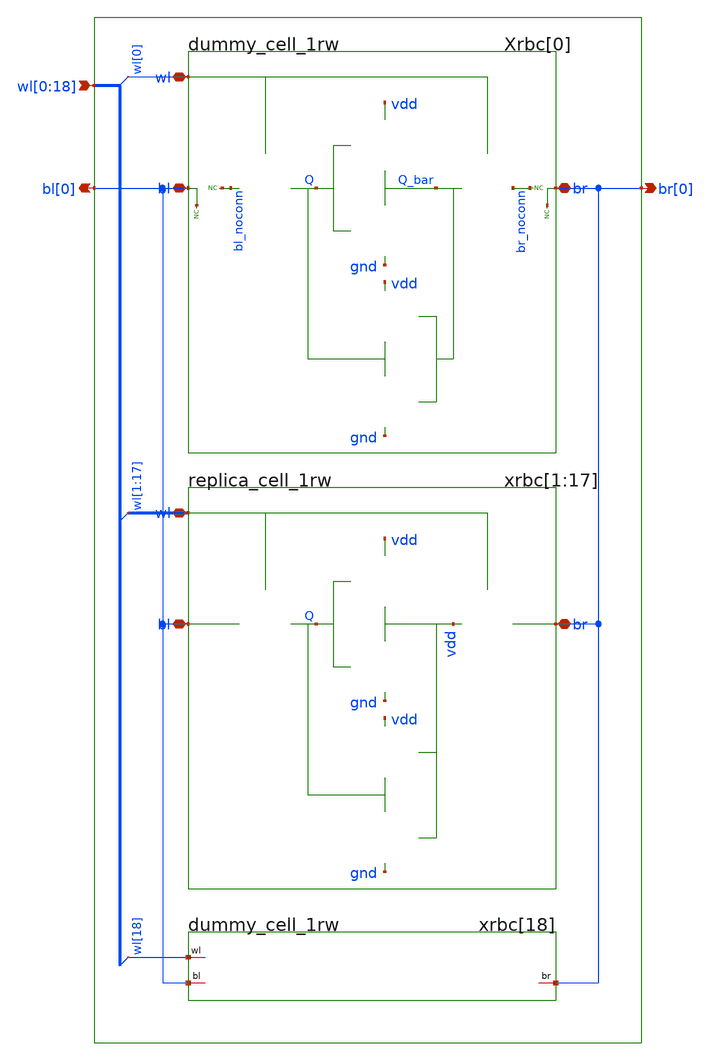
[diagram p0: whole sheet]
** sch_path: sram_4_16_scn4m/replica_column.sch
**.subckt replica_column bl[0] br[0]
*+ wl[0],wl[1],wl[2],wl[3],wl[4],wl[5],wl[6],wl[7],wl[8],wl[9],wl[10],wl[11],wl[12],wl[13],wl[14],wl[15],wl[16],wl[17],wl[18]
*.opin bl[0]
*.opin br[0]
*.ipin
*+ wl[0],wl[1],wl[2],wl[3],wl[4],wl[5],wl[6],wl[7],wl[8],wl[9],wl[10],wl[11],wl[12],wl[13],wl[14],wl[15],wl[16],wl[17],wl[18]
Xrbc[0] bl[0] br[0] wl[0] vdd gnd dummy_cell_1rw
xrbc[1] bl[0] br[0] wl[1] vdd gnd replica_cell_1rw
xrbc[2] bl[0] br[0] wl[2] vdd gnd replica_cell_1rw
xrbc[3] bl[0] br[0] wl[3] vdd gnd replica_cell_1rw
xrbc[4] bl[0] br[0] wl[4] vdd gnd replica_cell_1rw
xrbc[5] bl[0] br[0] wl[5] vdd gnd replica_cell_1rw
xrbc[6] bl[0] br[0] wl[6] vdd gnd replica_cell_1rw
xrbc[7] bl[0] br[0] wl[7] vdd gnd replica_cell_1rw
xrbc[8] bl[0] br[0] wl[8] vdd gnd replica_cell_1rw
xrbc[9] bl[0] br[0] wl[9] vdd gnd replica_cell_1rw
xrbc[10] bl[0] br[0] wl[10] vdd gnd replica_cell_1rw
xrbc[11] bl[0] br[0] wl[11] vdd gnd replica_cell_1rw
xrbc[12] bl[0] br[0] wl[12] vdd gnd replica_cell_1rw
xrbc[13] bl[0] br[0] wl[13] vdd gnd replica_cell_1rw
xrbc[14] bl[0] br[0] wl[14] vdd gnd replica_cell_1rw
xrbc[15] bl[0] br[0] wl[15] vdd gnd replica_cell_1rw
xrbc[16] bl[0] br[0] wl[16] vdd gnd replica_cell_1rw
xrbc[17] bl[0] br[0] wl[17] vdd gnd replica_cell_1rw
xrbc[18] bl[0] br[0] wl[18] vdd gnd dummy_cell_1rw
**.ends

* expanding   symbol:  dummy_cell_1rw.sch # of pins=3
** sym_path: sram_4_16_scn4m/dummy_cell_1rw.sch
** sch_path: sram_4_16_scn4m/dummy_cell_1rw.sch
.subckt dummy_cell_1rw bl br wl vdd gnd
*.iopin bl
*.iopin br
*.iopin wl
XM1004 Q wl bl_noconn gnd sky130_fd_pr__nfet_01v8 L=0.4 W=0.8 nf=1 ad='int((nf+1)/2) * W/nf * 0.29' as='int((nf+2)/2) * W/nf * 0.29'
+ pd='2*int((nf+1)/2) * (W/nf + 0.29)' ps='2*int((nf+2)/2) * (W/nf + 0.29)' nrd='0.29 / W' nrs='0.29 / W'
+ sa=0 sb=0 sd=0 mult=1 m=1
XM1001 Q_bar Q vdd vdd sky130_fd_pr__pfet_01v8 L=0.8 W=0.6 nf=1 ad='int((nf+1)/2) * W/nf * 0.29' as='int((nf+2)/2) * W/nf * 0.29'
+ pd='2*int((nf+1)/2) * (W/nf + 0.29)' ps='2*int((nf+2)/2) * (W/nf + 0.29)' nrd='0.29 / W' nrs='0.29 / W'
+ sa=0 sb=0 sd=0 mult=1 m=1
XM1003 Q_bar Q gnd gnd sky130_fd_pr__nfet_01v8 L=0.4 W=1.6 nf=1 ad='int((nf+1)/2) * W/nf * 0.29' as='int((nf+2)/2) * W/nf * 0.29'
+ pd='2*int((nf+1)/2) * (W/nf + 0.29)' ps='2*int((nf+2)/2) * (W/nf + 0.29)' nrd='0.29 / W' nrs='0.29 / W'
+ sa=0 sb=0 sd=0 mult=1 m=1
XM1002 Q Q_bar gnd gnd sky130_fd_pr__nfet_01v8 L=0.4 W=1.6 nf=1 ad='int((nf+1)/2) * W/nf * 0.29' as='int((nf+2)/2) * W/nf * 0.29'
+ pd='2*int((nf+1)/2) * (W/nf + 0.29)' ps='2*int((nf+2)/2) * (W/nf + 0.29)' nrd='0.29 / W' nrs='0.29 / W'
+ sa=0 sb=0 sd=0 mult=1 m=1
XM1000 Q Q_bar vdd vdd sky130_fd_pr__pfet_01v8 L=0.8 W=0.6 nf=1 ad='int((nf+1)/2) * W/nf * 0.29' as='int((nf+2)/2) * W/nf * 0.29'
+ pd='2*int((nf+1)/2) * (W/nf + 0.29)' ps='2*int((nf+2)/2) * (W/nf + 0.29)' nrd='0.29 / W' nrs='0.29 / W'
+ sa=0 sb=0 sd=0 mult=1 m=1
XM1005 br_noconn wl Q_bar gnd sky130_fd_pr__nfet_01v8 L=0.4 W=0.8 nf=1 ad='int((nf+1)/2) * W/nf * 0.29'
+ as='int((nf+2)/2) * W/nf * 0.29' pd='2*int((nf+1)/2) * (W/nf + 0.29)' ps='2*int((nf+2)/2) * (W/nf + 0.29)'
+ nrd='0.29 / W' nrs='0.29 / W' sa=0 sb=0 sd=0 mult=1 m=1
* noconn bl_noconn
* noconn br_noconn
* noconn br
* noconn bl
.ends


* expanding   symbol:  replica_cell_1rw.sch # of pins=3
** sym_path: sram_4_16_scn4m/replica_cell_1rw.sch
** sch_path: sram_4_16_scn4m/replica_cell_1rw.sch
.subckt replica_cell_1rw bl br wl vdd gnd
*.iopin bl
*.iopin br
*.iopin wl
XM1004 Q wl bl gnd sky130_fd_pr__nfet_01v8 L=0.4 W=0.8 nf=1 ad='int((nf+1)/2) * W/nf * 0.29' as='int((nf+2)/2) * W/nf * 0.29'
+ pd='2*int((nf+1)/2) * (W/nf + 0.29)' ps='2*int((nf+2)/2) * (W/nf + 0.29)' nrd='0.29 / W' nrs='0.29 / W'
+ sa=0 sb=0 sd=0 mult=1 m=1
XM1001 vdd Q vdd vdd sky130_fd_pr__pfet_01v8 L=0.8 W=0.6 nf=1 ad='int((nf+1)/2) * W/nf * 0.29' as='int((nf+2)/2) * W/nf * 0.29'
+ pd='2*int((nf+1)/2) * (W/nf + 0.29)' ps='2*int((nf+2)/2) * (W/nf + 0.29)' nrd='0.29 / W' nrs='0.29 / W'
+ sa=0 sb=0 sd=0 mult=1 m=1
XM1003 vdd Q gnd gnd sky130_fd_pr__nfet_01v8 L=0.4 W=1.6 nf=1 ad='int((nf+1)/2) * W/nf * 0.29' as='int((nf+2)/2) * W/nf * 0.29'
+ pd='2*int((nf+1)/2) * (W/nf + 0.29)' ps='2*int((nf+2)/2) * (W/nf + 0.29)' nrd='0.29 / W' nrs='0.29 / W'
+ sa=0 sb=0 sd=0 mult=1 m=1
XM1002 Q vdd gnd gnd sky130_fd_pr__nfet_01v8 L=0.4 W=1.6 nf=1 ad='int((nf+1)/2) * W/nf * 0.29' as='int((nf+2)/2) * W/nf * 0.29'
+ pd='2*int((nf+1)/2) * (W/nf + 0.29)' ps='2*int((nf+2)/2) * (W/nf + 0.29)' nrd='0.29 / W' nrs='0.29 / W'
+ sa=0 sb=0 sd=0 mult=1 m=1
XM1000 Q vdd vdd vdd sky130_fd_pr__pfet_01v8 L=0.8 W=0.6 nf=1 ad='int((nf+1)/2) * W/nf * 0.29' as='int((nf+2)/2) * W/nf * 0.29'
+ pd='2*int((nf+1)/2) * (W/nf + 0.29)' ps='2*int((nf+2)/2) * (W/nf + 0.29)' nrd='0.29 / W' nrs='0.29 / W'
+ sa=0 sb=0 sd=0 mult=1 m=1
XM1005 br wl vdd gnd sky130_fd_pr__nfet_01v8 L=0.4 W=0.8 nf=1 ad='int((nf+1)/2) * W/nf * 0.29' as='int((nf+2)/2) * W/nf * 0.29'
+ pd='2*int((nf+1)/2) * (W/nf + 0.29)' ps='2*int((nf+2)/2) * (W/nf + 0.29)' nrd='0.29 / W' nrs='0.29 / W'
+ sa=0 sb=0 sd=0 mult=1 m=1
.ends

.end
